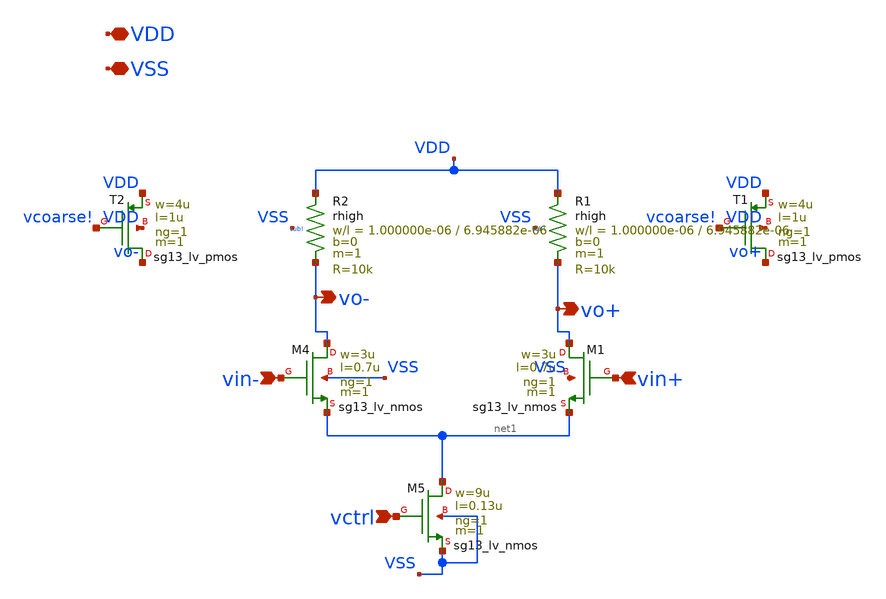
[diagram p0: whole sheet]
** sch_path: xschem/ring_inverter.sch
**.subckt ring_inverter VDD VSS vo+ vin- vctrl vo- vin+
*.iopin VDD
*.iopin VSS
*.opin vo+
*.ipin vin-
*.ipin vctrl
*.opin vo-
*.ipin vin+
XM4 vo- vin- net1 VSS sg13_lv_nmos w=3u l=0.7u ng=1 m=1 mm_ok=1
XM5 net1 vctrl VSS VSS sg13_lv_nmos w=9u l=0.13u ng=1 m=1 mm_ok=1
XM1 vo+ vin+ net1 VSS sg13_lv_nmos w=3u l=0.7u ng=1 m=1 mm_ok=1
XR1 VDD vo+ sub! rhigh w=1.000000e-06 l=6.945882e-06 m=1 b=0 mm_ok=1
XR2 VDD vo- sub! rhigh w=1.000000e-06 l=6.945882e-06 m=1 b=0 mm_ok=1
XT1 vo+ vcoarse! VDD VDD sg13_lv_pmos w=4u l=1u ng=1 m=1 mm_ok=1
XT2 vo- vcoarse! VDD VDD sg13_lv_pmos w=4u l=1u ng=1 m=1 mm_ok=1
**.ends
.end
